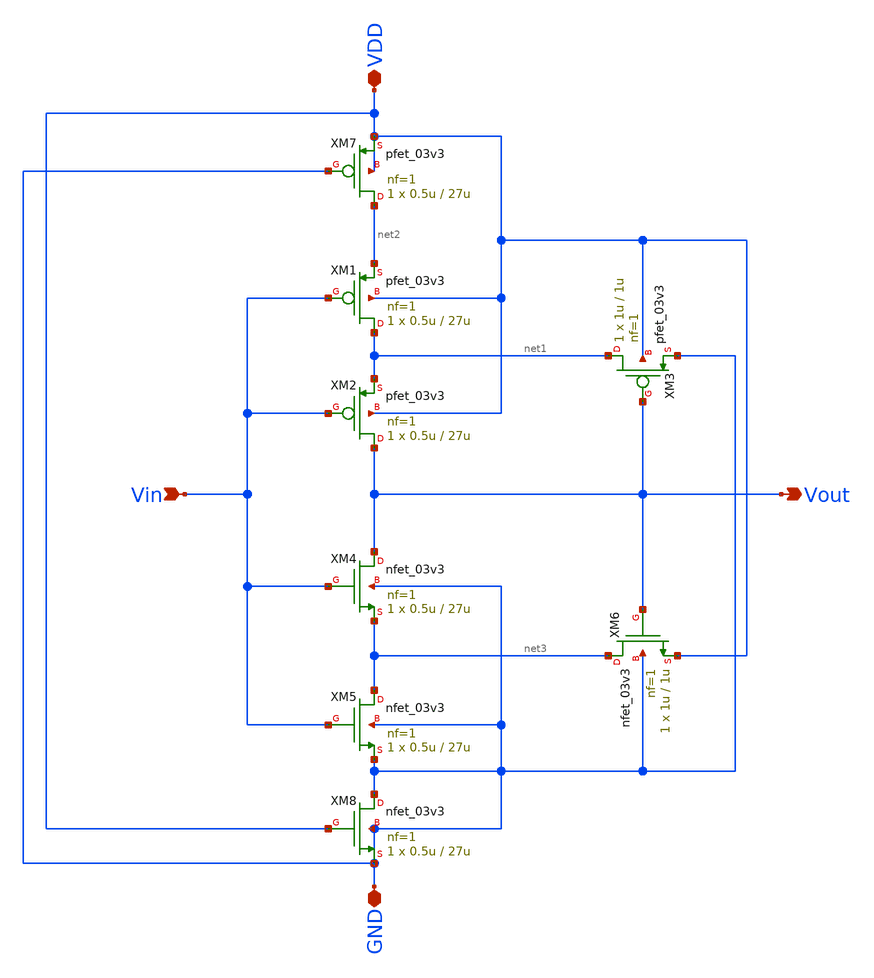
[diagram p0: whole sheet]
** sch_path: analog/clock/sch/B04_schmitt_trigger.sch
**.subckt B04_schmitt_trigger VDD GND Vin Vout
*.iopin VDD
*.iopin GND
*.ipin Vin
*.opin Vout
XM1 net1 Vin net2 VDD pfet_03v3 L=27u W=0.5u nf=1 ad='int((nf+1)/2) * W/nf * 0.18u' as='int((nf+2)/2) * W/nf * 0.18u'
+ pd='2*int((nf+1)/2) * (W/nf + 0.18u)' ps='2*int((nf+2)/2) * (W/nf + 0.18u)' nrd='0.18u / W' nrs='0.18u / W'
+ sa=0 sb=0 sd=0 m=1
XM2 Vout Vin net1 VDD pfet_03v3 L=27u W=0.5u nf=1 ad='int((nf+1)/2) * W/nf * 0.18u' as='int((nf+2)/2) * W/nf * 0.18u'
+ pd='2*int((nf+1)/2) * (W/nf + 0.18u)' ps='2*int((nf+2)/2) * (W/nf + 0.18u)' nrd='0.18u / W' nrs='0.18u / W'
+ sa=0 sb=0 sd=0 m=1
XM3 net1 Vout GND VDD pfet_03v3 L=1u W=1u nf=1 ad='int((nf+1)/2) * W/nf * 0.18u' as='int((nf+2)/2) * W/nf * 0.18u'
+ pd='2*int((nf+1)/2) * (W/nf + 0.18u)' ps='2*int((nf+2)/2) * (W/nf + 0.18u)' nrd='0.18u / W' nrs='0.18u / W'
+ sa=0 sb=0 sd=0 m=1
XM4 Vout Vin net3 GND nfet_03v3 L=27u W=0.5u nf=1 ad='int((nf+1)/2) * W/nf * 0.18u' as='int((nf+2)/2) * W/nf * 0.18u'
+ pd='2*int((nf+1)/2) * (W/nf + 0.18u)' ps='2*int((nf+2)/2) * (W/nf + 0.18u)' nrd='0.18u / W' nrs='0.18u / W'
+ sa=0 sb=0 sd=0 m=1
XM5 net3 Vin GND GND nfet_03v3 L=27u W=0.5u nf=1 ad='int((nf+1)/2) * W/nf * 0.18u' as='int((nf+2)/2) * W/nf * 0.18u'
+ pd='2*int((nf+1)/2) * (W/nf + 0.18u)' ps='2*int((nf+2)/2) * (W/nf + 0.18u)' nrd='0.18u / W' nrs='0.18u / W'
+ sa=0 sb=0 sd=0 m=1
XM6 net3 Vout VDD GND nfet_03v3 L=1u W=1u nf=1 ad='int((nf+1)/2) * W/nf * 0.18u' as='int((nf+2)/2) * W/nf * 0.18u'
+ pd='2*int((nf+1)/2) * (W/nf + 0.18u)' ps='2*int((nf+2)/2) * (W/nf + 0.18u)' nrd='0.18u / W' nrs='0.18u / W'
+ sa=0 sb=0 sd=0 m=1
XM7 net2 GND VDD VDD pfet_03v3 L=27u W=0.5u nf=1 ad='int((nf+1)/2) * W/nf * 0.18u' as='int((nf+2)/2) * W/nf * 0.18u'
+ pd='2*int((nf+1)/2) * (W/nf + 0.18u)' ps='2*int((nf+2)/2) * (W/nf + 0.18u)' nrd='0.18u / W' nrs='0.18u / W'
+ sa=0 sb=0 sd=0 m=1
XM8 GND VDD GND GND nfet_03v3 L=27u W=0.5u nf=1 ad='int((nf+1)/2) * W/nf * 0.18u' as='int((nf+2)/2) * W/nf * 0.18u'
+ pd='2*int((nf+1)/2) * (W/nf + 0.18u)' ps='2*int((nf+2)/2) * (W/nf + 0.18u)' nrd='0.18u / W' nrs='0.18u / W'
+ sa=0 sb=0 sd=0 m=1
**.ends
.end
